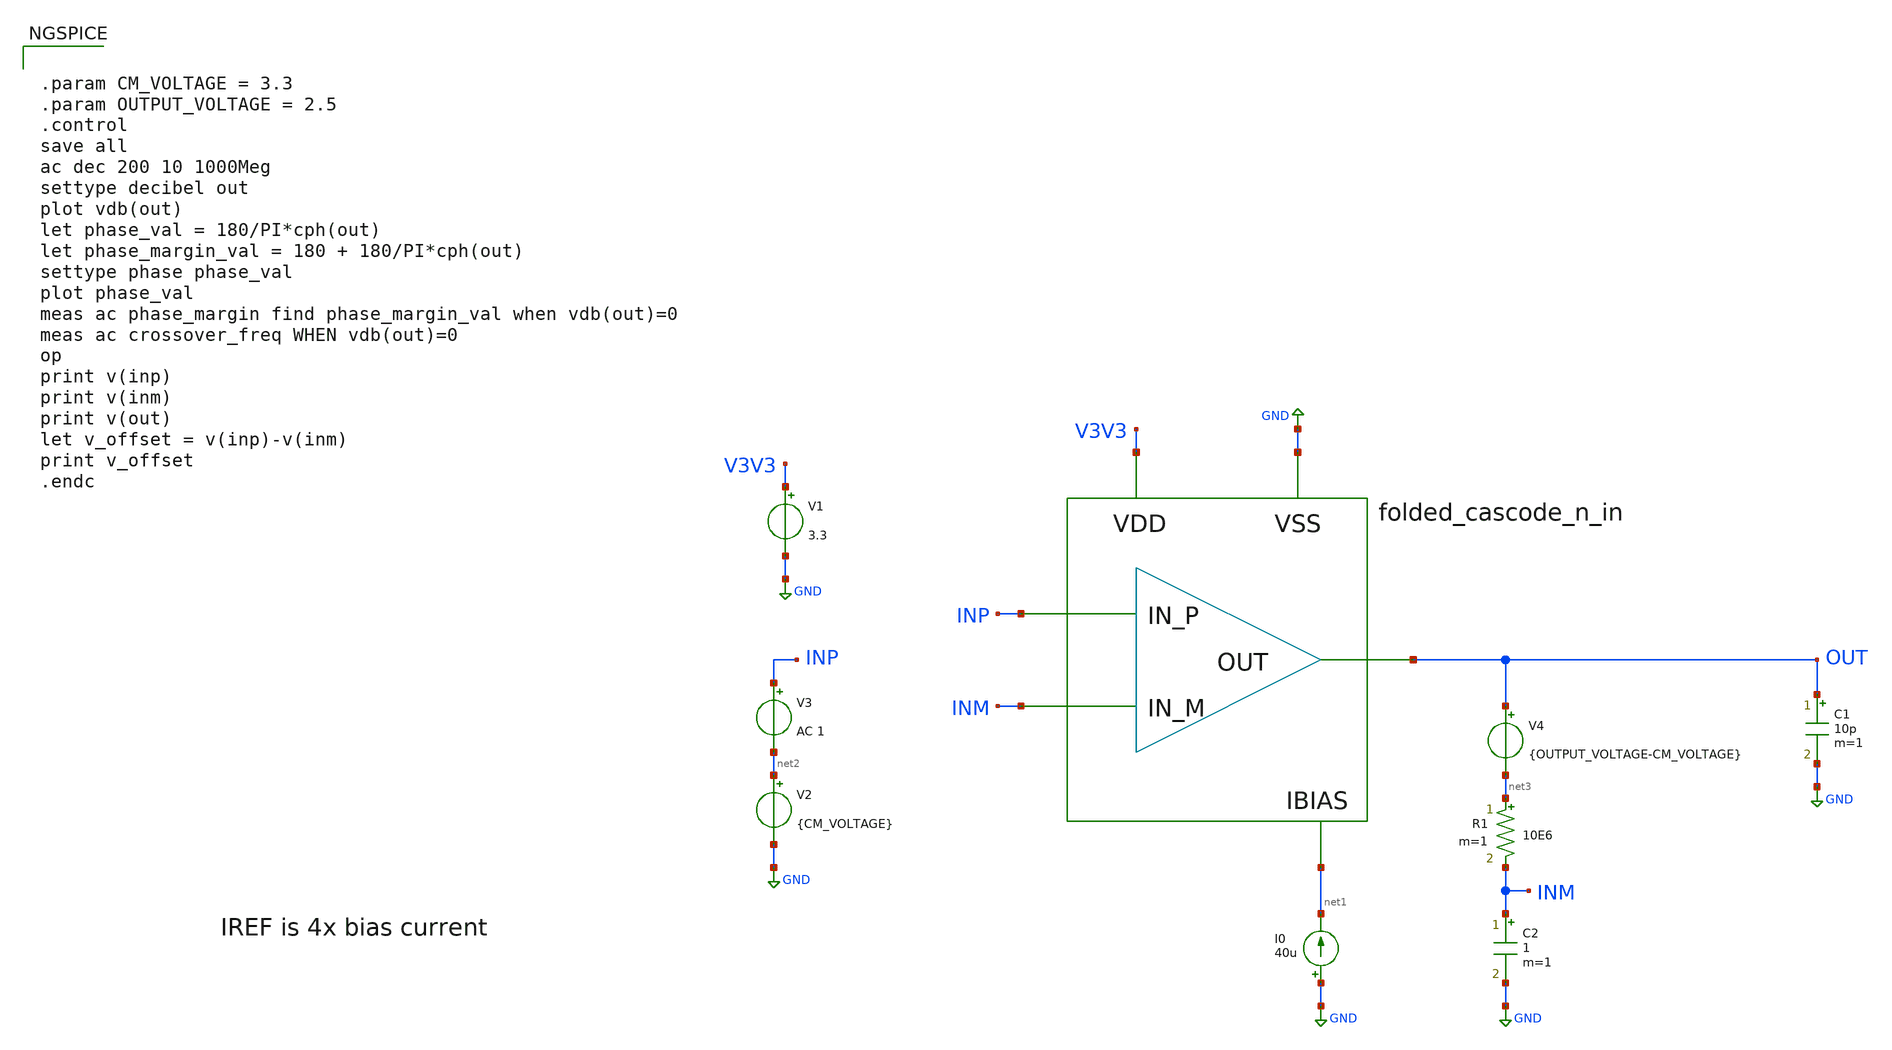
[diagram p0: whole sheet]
** sch_path: images/foss-asic-tools/addons/examples/open-pmic/design/folded-cascode-n-in/folded_cascode_n_in_tb.sch
**.subckt folded_cascode_n_in_tb
V1 V3V3 GND 3.3
I0 GND net1 40u
x1 INP INM OUT V3V3 GND net1 folded_cascode_n_in
V2 net2 GND {CM_VOLTAGE}
V3 INP net2 AC 1
C1 OUT GND 10p m=1
R1 net3 INM 10E6 m=1
V4 OUT net3 {OUTPUT_VOLTAGE-CM_VOLTAGE}
C2 INM GND 1 m=1
**** begin user architecture code


.param CM_VOLTAGE = 3.3
.param OUTPUT_VOLTAGE = 2.5
.control
save all
ac dec 200 10 1000Meg
settype decibel out
plot vdb(out)
let phase_val = 180/PI*cph(out)
let phase_margin_val = 180 + 180/PI*cph(out)
settype phase phase_val
plot phase_val
meas ac phase_margin find phase_margin_val when vdb(out)=0
meas ac crossover_freq WHEN vdb(out)=0
op
print v(inp)
print v(inm)
print v(out)
let v_offset = v(inp)-v(inm)
print v_offset
.endc



.include $::SKYWATER_MODELS/cells/nfet_01v8/sky130_fd_pr__nfet_01v8__tt.corner.spice
.include $::SKYWATER_MODELS/cells/nfet_01v8_lvt/sky130_fd_pr__nfet_01v8_lvt__tt.corner.spice
.include $::SKYWATER_MODELS/cells/pfet_01v8/sky130_fd_pr__pfet_01v8__tt.corner.spice
.include $::SKYWATER_MODELS/cells/nfet_03v3_nvt/sky130_fd_pr__nfet_03v3_nvt__tt.corner.spice
.include $::SKYWATER_MODELS/cells/nfet_05v0_nvt/sky130_fd_pr__nfet_05v0_nvt__tt.corner.spice
.include $::SKYWATER_MODELS/cells/esd_nfet_01v8/sky130_fd_pr__esd_nfet_01v8__tt.corner.spice
.include $::SKYWATER_MODELS/cells/pfet_01v8_lvt/sky130_fd_pr__pfet_01v8_lvt__tt.corner.spice
.include $::SKYWATER_MODELS/cells/pfet_01v8_hvt/sky130_fd_pr__pfet_01v8_hvt__tt.corner.spice
.include $::SKYWATER_MODELS/cells/esd_pfet_g5v0d10v5/sky130_fd_pr__esd_pfet_g5v0d10v5__tt.corner.spice
.include $::SKYWATER_MODELS/cells/pfet_g5v0d10v5/sky130_fd_pr__pfet_g5v0d10v5__tt.corner.spice
.include $::SKYWATER_MODELS/cells/pfet_g5v0d16v0/sky130_fd_pr__pfet_g5v0d16v0__tt.corner.spice
.include $::SKYWATER_MODELS/cells/nfet_g5v0d10v5/sky130_fd_pr__nfet_g5v0d10v5__tt.corner.spice
.include $::SKYWATER_MODELS/cells/nfet_g5v0d16v0/sky130_fd_pr__nfet_g5v0d16v0__tt_discrete.corner.spice
.include $::SKYWATER_MODELS/cells/esd_nfet_g5v0d10v5/sky130_fd_pr__esd_nfet_g5v0d10v5__tt.corner.spice
.include $::SKYWATER_MODELS/models/corners/tt/nonfet.spice
* Mismatch parameters
.include $::SKYWATER_MODELS/cells/nfet_01v8/sky130_fd_pr__nfet_01v8__mismatch.corner.spice
.include $::SKYWATER_MODELS/cells/pfet_01v8/sky130_fd_pr__pfet_01v8__mismatch.corner.spice
.include $::SKYWATER_MODELS/cells/nfet_01v8_lvt/sky130_fd_pr__nfet_01v8_lvt__mismatch.corner.spice
.include $::SKYWATER_MODELS/cells/pfet_01v8_lvt/sky130_fd_pr__pfet_01v8_lvt__mismatch.corner.spice
.include $::SKYWATER_MODELS/cells/pfet_01v8_hvt/sky130_fd_pr__pfet_01v8_hvt__mismatch.corner.spice
.include $::SKYWATER_MODELS/cells/nfet_g5v0d10v5/sky130_fd_pr__nfet_g5v0d10v5__mismatch.corner.spice
.include $::SKYWATER_MODELS/cells/pfet_g5v0d10v5/sky130_fd_pr__pfet_g5v0d10v5__mismatch.corner.spice
.include $::SKYWATER_MODELS/cells/nfet_05v0_nvt/sky130_fd_pr__nfet_05v0_nvt__mismatch.corner.spice
.include $::SKYWATER_MODELS/cells/nfet_03v3_nvt/sky130_fd_pr__nfet_03v3_nvt__mismatch.corner.spice
* Resistor$::SKYWATER_MODELS/Capacitor
.include $::SKYWATER_MODELS/models/r+c/res_typical__cap_typical.spice
.include $::SKYWATER_MODELS/models/r+c/res_typical__cap_typical__lin.spice
* Special cells
.include $::SKYWATER_MODELS/models/corners/tt/specialized_cells.spice
* All models
.include $::SKYWATER_MODELS/models/all.spice
* Corner
.include $::SKYWATER_MODELS/models/corners/tt/rf.spice

**** end user architecture code
**.ends
.GLOBAL GND
**** begin user architecture code
[sky130_models]
**** end user architecture code
.end
